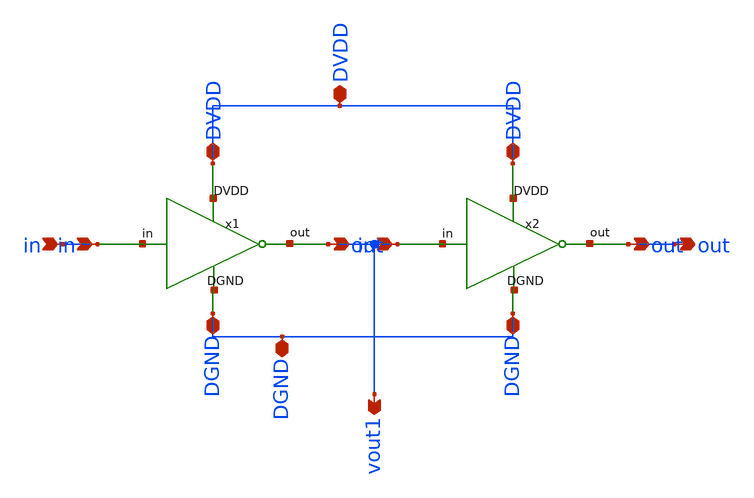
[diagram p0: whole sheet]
** sch_path: assignments/assignment4/inv_tb.sch
**.subckt inv_tb DGND in out DVDD vout1
*.iopin DGND
*.ipin in
*.opin out
*.iopin DVDD
*.opin vout1
x1 DVDD in vout1 DGND inv
x2 DVDD vout1 out DGND inv
**.ends

* expanding   symbol:  inv.sym # of pins=8
** sym_path: assignments/assignment4/inv.sym
** sch_path: assignments/assignment4/inv.sch
.subckt inv DVDD in out DGND
*.ipin in
*.opin out
*.iopin DVDD
*.iopin DGND
XM3 out in DVDD DVDD sky130_fd_pr__pfet_01v8 L=0.15 W=0.84 nf=1 ad='int((nf+1)/2) * W/nf * 0.29' as='int((nf+2)/2) * W/nf * 0.29'
+ pd='2*int((nf+1)/2) * (W/nf + 0.29)' ps='2*int((nf+2)/2) * (W/nf + 0.29)' nrd='0.29 / W' nrs='0.29 / W'
+ sa=0 sb=0 sd=0 mult=1 m=1
XM2 out in DGND DGND sky130_fd_pr__nfet_01v8 L=0.15 W=0.42 nf=1 ad='int((nf+1)/2) * W/nf * 0.29' as='int((nf+2)/2) * W/nf * 0.29'
+ pd='2*int((nf+1)/2) * (W/nf + 0.29)' ps='2*int((nf+2)/2) * (W/nf + 0.29)' nrd='0.29 / W' nrs='0.29 / W'
+ sa=0 sb=0 sd=0 mult=1 m=1
.ends

.end
